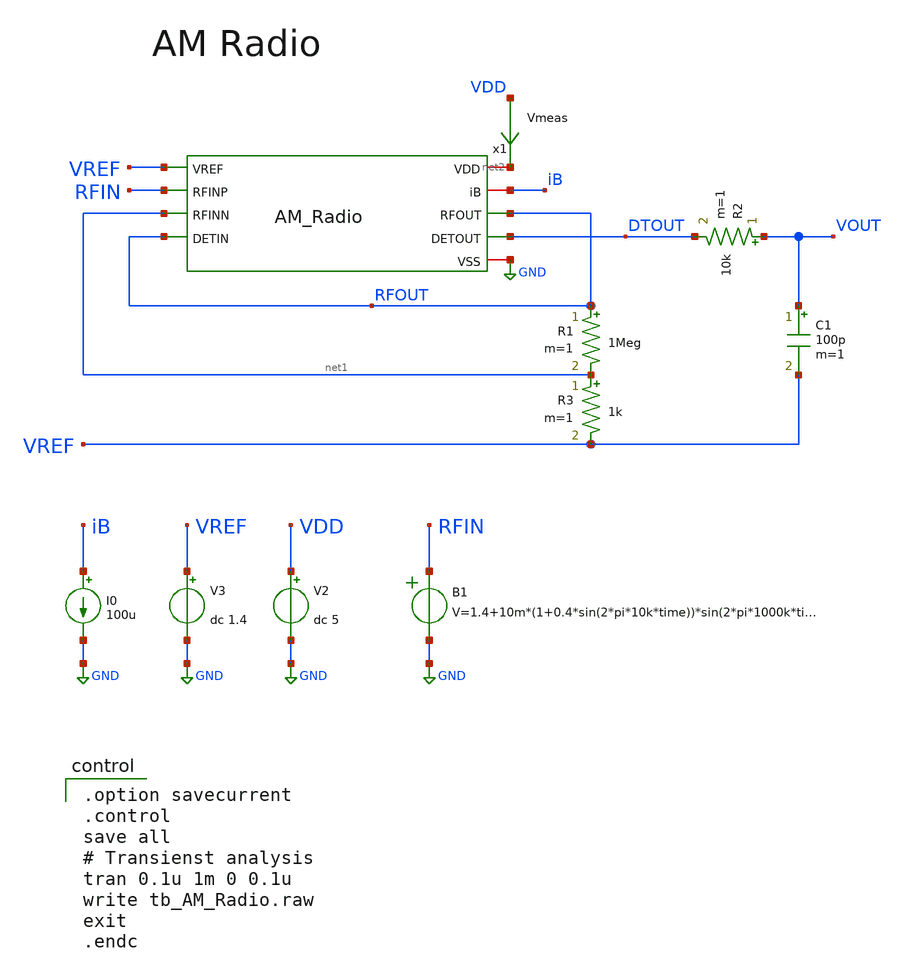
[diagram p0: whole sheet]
** sch_path: member_project/AM_Radio/Yamada3/xschem/tb_AM_Radio.sch
**.subckt tb_AM_Radio
V2 VDD GND dc 5
V3 VREF GND dc 1.4
B1 RFIN GND V=1.4+10m*(1+0.4*sin(2*pi*10k*time))*sin(2*pi*1000k*time)
R2 VOUT DTOUT 10k m=1
I0 iB GND 100u
C1 VOUT VREF 100p m=1
x1 net2 iB VREF RFIN net1 RFOUT RFOUT DTOUT GND AM_Radio
R1 RFOUT net1 1Meg m=1
Vmeas VDD net2 0
.save i(vmeas)
R3 net1 VREF 1k m=1
**** begin user architecture code
 .include $::LIB/ip62_models

.option savecurrent
.control
save all
# Transienst analysis
tran 0.1u 1m 0 0.1u
write tb_AM_Radio.raw
exit
.endc

**** end user architecture code
**.ends
.GLOBAL GND
.end
